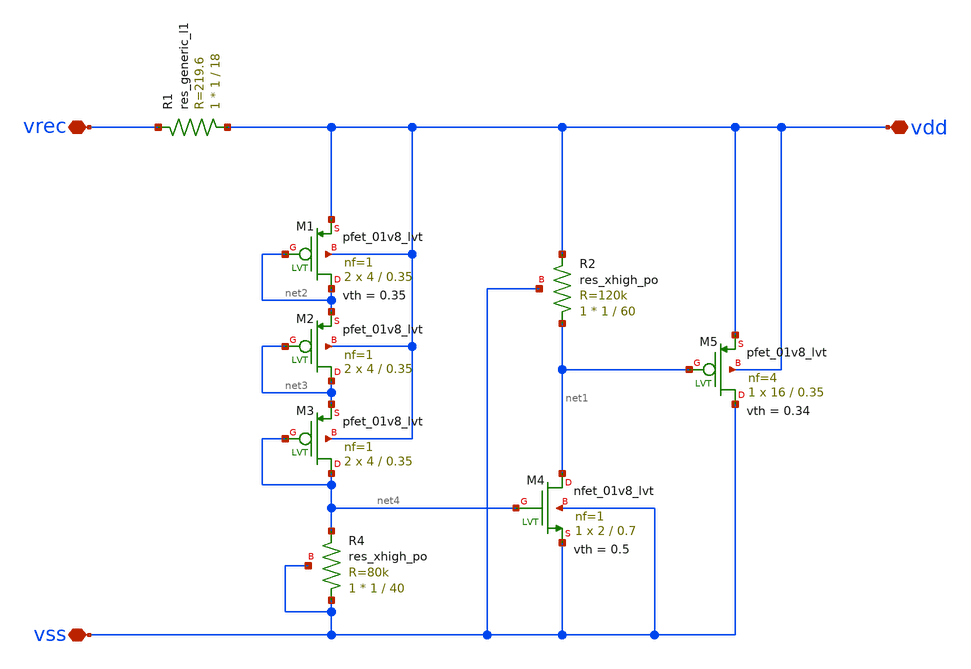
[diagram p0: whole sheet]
** sch_path: XSCHEM/voltage_limiter.sch
**.subckt voltage_limiter vss vrec vdd
*.iopin vss
*.iopin vrec
*.iopin vdd
XM4 net1 net4 vss vss sky130_fd_pr__nfet_01v8_lvt L=0.7 W=2 nf=1 ad='int((nf+1)/2) * W/nf * 0.29' as='int((nf+2)/2) * W/nf * 0.29'
+ pd='2*int((nf+1)/2) * (W/nf + 0.29)' ps='2*int((nf+2)/2) * (W/nf + 0.29)' nrd='0.29 / W' nrs='0.29 / W'
+ sa=0 sb=0 sd=0 mult=1 m=1
XM5 vss net1 vdd vdd sky130_fd_pr__pfet_01v8_lvt L=0.35 W=16 nf=4 ad='int((nf+1)/2) * W/nf * 0.29' as='int((nf+2)/2) * W/nf * 0.29'
+ pd='2*int((nf+1)/2) * (W/nf + 0.29)' ps='2*int((nf+2)/2) * (W/nf + 0.29)' nrd='0.29 / W' nrs='0.29 / W'
+ sa=0 sb=0 sd=0 mult=1 m=1
XM1 net2 net2 vdd vdd sky130_fd_pr__pfet_01v8_lvt L=0.35 W=4 nf=1 ad='int((nf+1)/2) * W/nf * 0.29' as='int((nf+2)/2) * W/nf * 0.29'
+ pd='2*int((nf+1)/2) * (W/nf + 0.29)' ps='2*int((nf+2)/2) * (W/nf + 0.29)' nrd='0.29 / W' nrs='0.29 / W'
+ sa=0 sb=0 sd=0 mult=2 m=2
XM2 net3 net3 net2 vdd sky130_fd_pr__pfet_01v8_lvt L=0.35 W=4 nf=1 ad='int((nf+1)/2) * W/nf * 0.29' as='int((nf+2)/2) * W/nf * 0.29'
+ pd='2*int((nf+1)/2) * (W/nf + 0.29)' ps='2*int((nf+2)/2) * (W/nf + 0.29)' nrd='0.29 / W' nrs='0.29 / W'
+ sa=0 sb=0 sd=0 mult=2 m=2
XM3 net4 net4 net3 vdd sky130_fd_pr__pfet_01v8_lvt L=0.35 W=4 nf=1 ad='int((nf+1)/2) * W/nf * 0.29' as='int((nf+2)/2) * W/nf * 0.29'
+ pd='2*int((nf+1)/2) * (W/nf + 0.29)' ps='2*int((nf+2)/2) * (W/nf + 0.29)' nrd='0.29 / W' nrs='0.29 / W'
+ sa=0 sb=0 sd=0 mult=2 m=2
XR2 net1 vdd vss sky130_fd_pr__res_xhigh_po W=1 L=60 mult=1 m=1
XR4 vss net4 vss sky130_fd_pr__res_xhigh_po W=1 L=40 mult=1 m=1
R1 vdd vrec sky130_fd_pr__res_generic_l1 W=1 L=18 m=1
**.ends
.end
